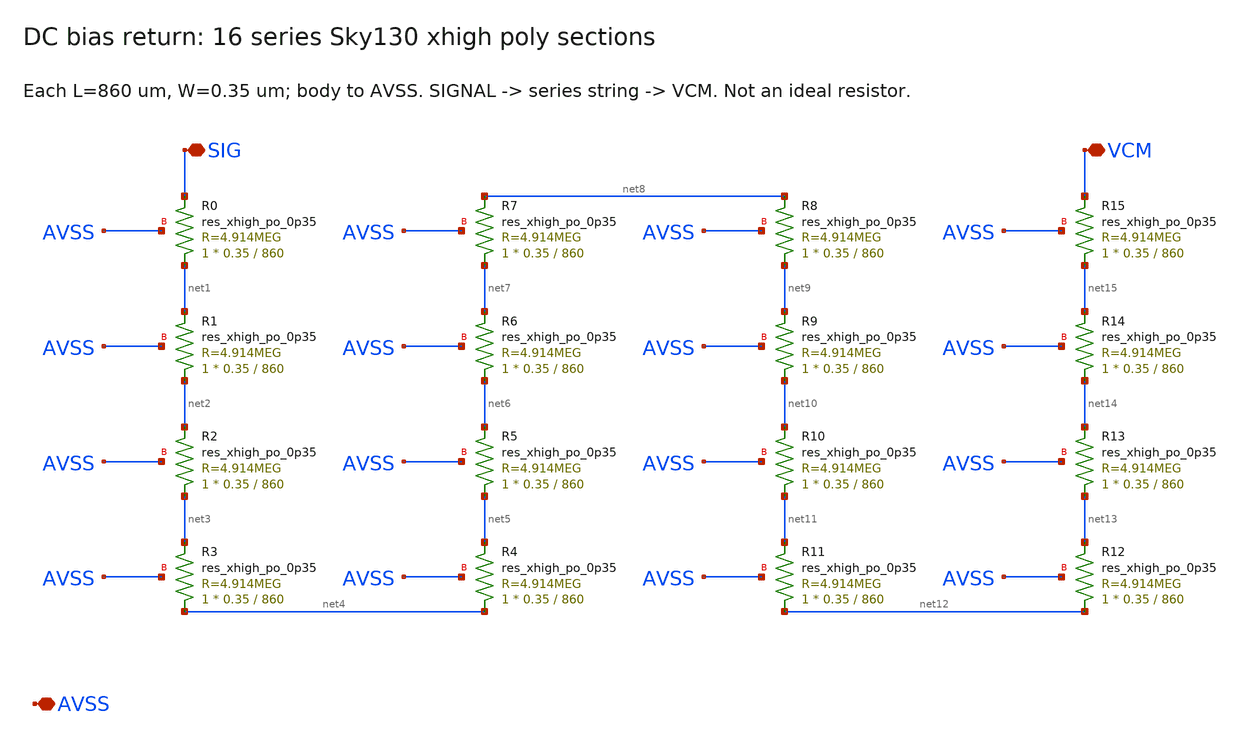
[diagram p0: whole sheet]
** sch_path: afe/xschem/tbci_bias_return.sch
**.subckt tbci_bias_return SIG VCM AVSS
*.iopin SIG
*.iopin VCM
*.iopin AVSS
XR0 net1 SIG AVSS sky130_fd_pr__res_xhigh_po_0p35 L=860 mult=1 m=1
XR1 net2 net1 AVSS sky130_fd_pr__res_xhigh_po_0p35 L=860 mult=1 m=1
XR2 net3 net2 AVSS sky130_fd_pr__res_xhigh_po_0p35 L=860 mult=1 m=1
XR3 net4 net3 AVSS sky130_fd_pr__res_xhigh_po_0p35 L=860 mult=1 m=1
XR4 net4 net5 AVSS sky130_fd_pr__res_xhigh_po_0p35 L=860 mult=1 m=1
XR5 net5 net6 AVSS sky130_fd_pr__res_xhigh_po_0p35 L=860 mult=1 m=1
XR6 net6 net7 AVSS sky130_fd_pr__res_xhigh_po_0p35 L=860 mult=1 m=1
XR7 net7 net8 AVSS sky130_fd_pr__res_xhigh_po_0p35 L=860 mult=1 m=1
XR8 net9 net8 AVSS sky130_fd_pr__res_xhigh_po_0p35 L=860 mult=1 m=1
XR9 net10 net9 AVSS sky130_fd_pr__res_xhigh_po_0p35 L=860 mult=1 m=1
XR10 net11 net10 AVSS sky130_fd_pr__res_xhigh_po_0p35 L=860 mult=1 m=1
XR11 net12 net11 AVSS sky130_fd_pr__res_xhigh_po_0p35 L=860 mult=1 m=1
XR12 net12 net13 AVSS sky130_fd_pr__res_xhigh_po_0p35 L=860 mult=1 m=1
XR13 net13 net14 AVSS sky130_fd_pr__res_xhigh_po_0p35 L=860 mult=1 m=1
XR14 net14 net15 AVSS sky130_fd_pr__res_xhigh_po_0p35 L=860 mult=1 m=1
XR15 net15 VCM AVSS sky130_fd_pr__res_xhigh_po_0p35 L=860 mult=1 m=1
**.ends
.end
